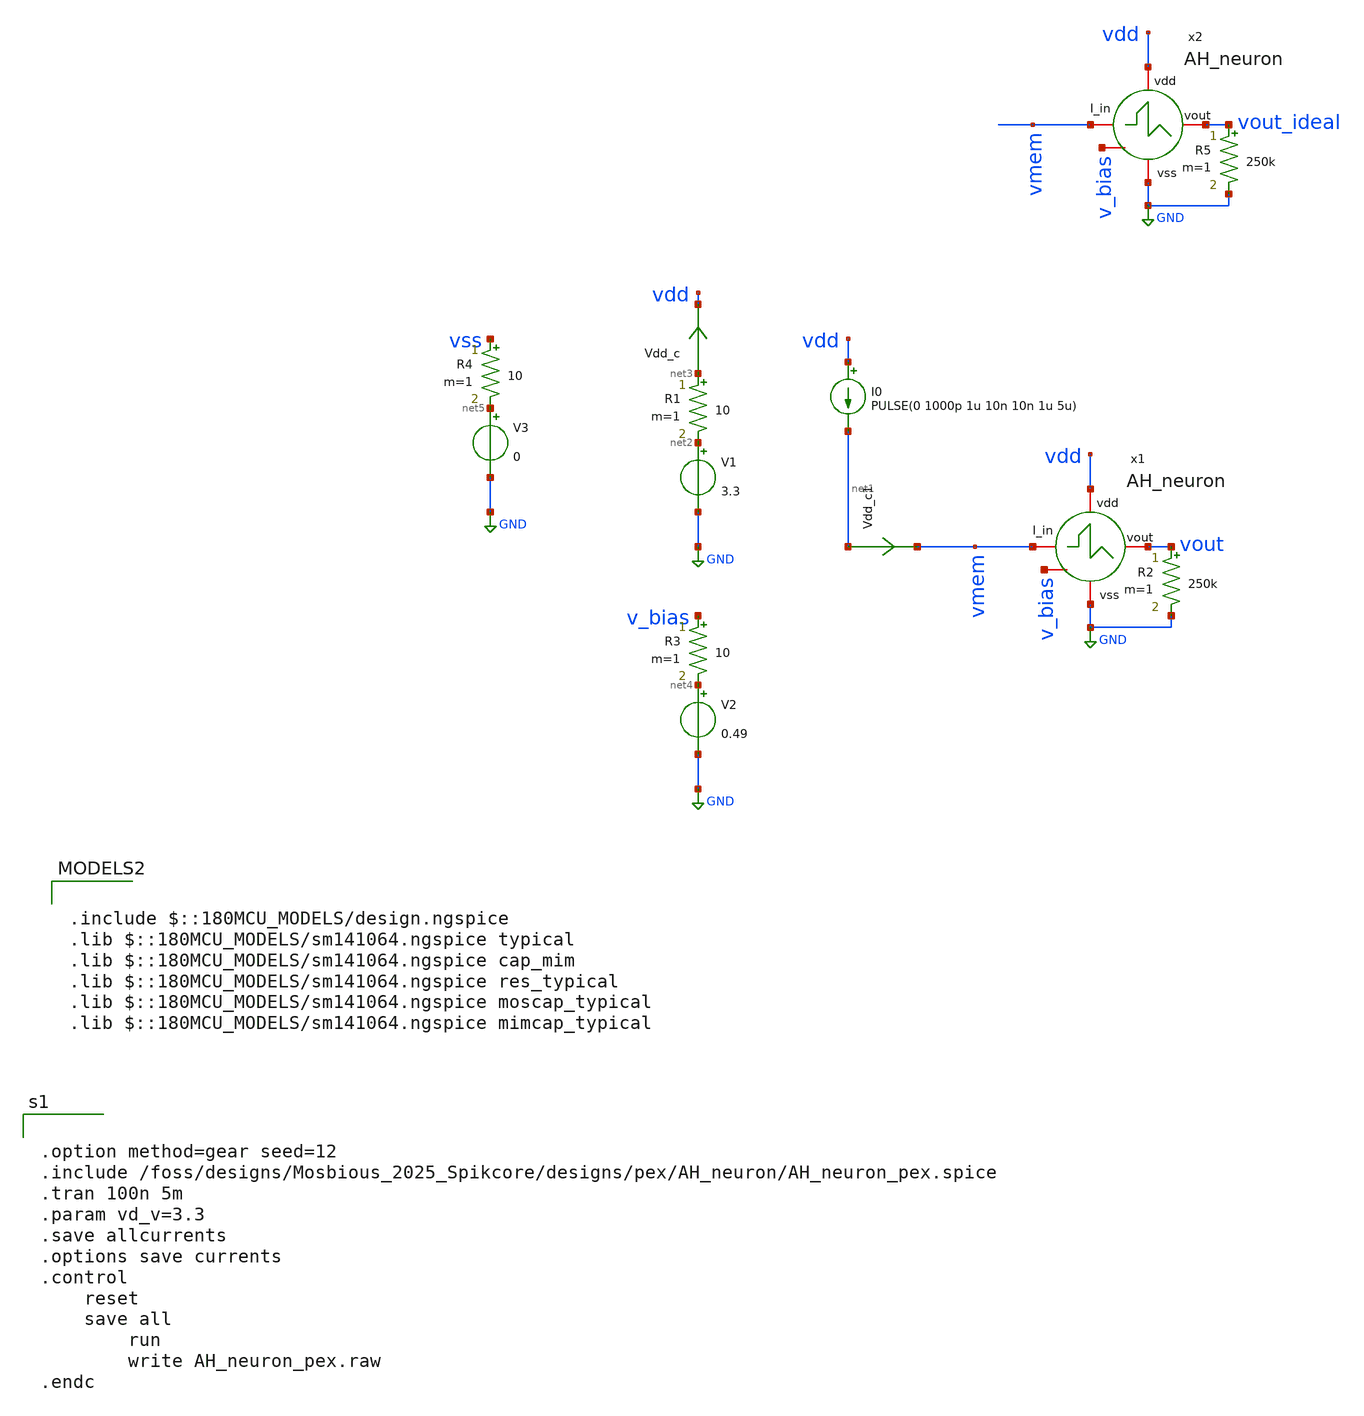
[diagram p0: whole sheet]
** sch_path: designs/pex/AH_neuron/AH_neuron_pex.sch
**.subckt AH_neuron_pex
V1 net2 GND 3.3
Vdd_c net3 vdd 0
.save i(vdd_c)
I0 vdd net1 PULSE(0 1000p 1u 10n 10n 1u 5u)
R1 net3 net2 10 m=1
R2 vout GND 250k m=1
Vdd_c1 net1 vmem 0
.save i(vdd_c1)
V2 net4 GND 0.49
R3 v_bias net4 10 m=1
V3 net5 GND 0
R4 vss net5 10 m=1
x1 vdd vmem vout GND v_bias AH_neuron
x2 vdd vmem vout_ideal GND v_bias AH_neuron
R5 vout_ideal GND 250k m=1
**** begin user architecture code


.option method=gear seed=12
.include /foss/designs/Mosbious_2025_Spikcore/designs/pex/AH_neuron/AH_neuron_pex.spice
.tran 100n 5m
.param vd_v=3.3
.save allcurrents
.options save currents
.control
	reset
	save all
        run
        write AH_neuron_pex.raw
.endc



.include $::180MCU_MODELS/design.ngspice
.lib $::180MCU_MODELS/sm141064.ngspice typical
.lib $::180MCU_MODELS/sm141064.ngspice cap_mim
.lib $::180MCU_MODELS/sm141064.ngspice res_typical
.lib $::180MCU_MODELS/sm141064.ngspice moscap_typical
.lib $::180MCU_MODELS/sm141064.ngspice mimcap_typical

**** end user architecture code
**.ends
.GLOBAL GND
.end
